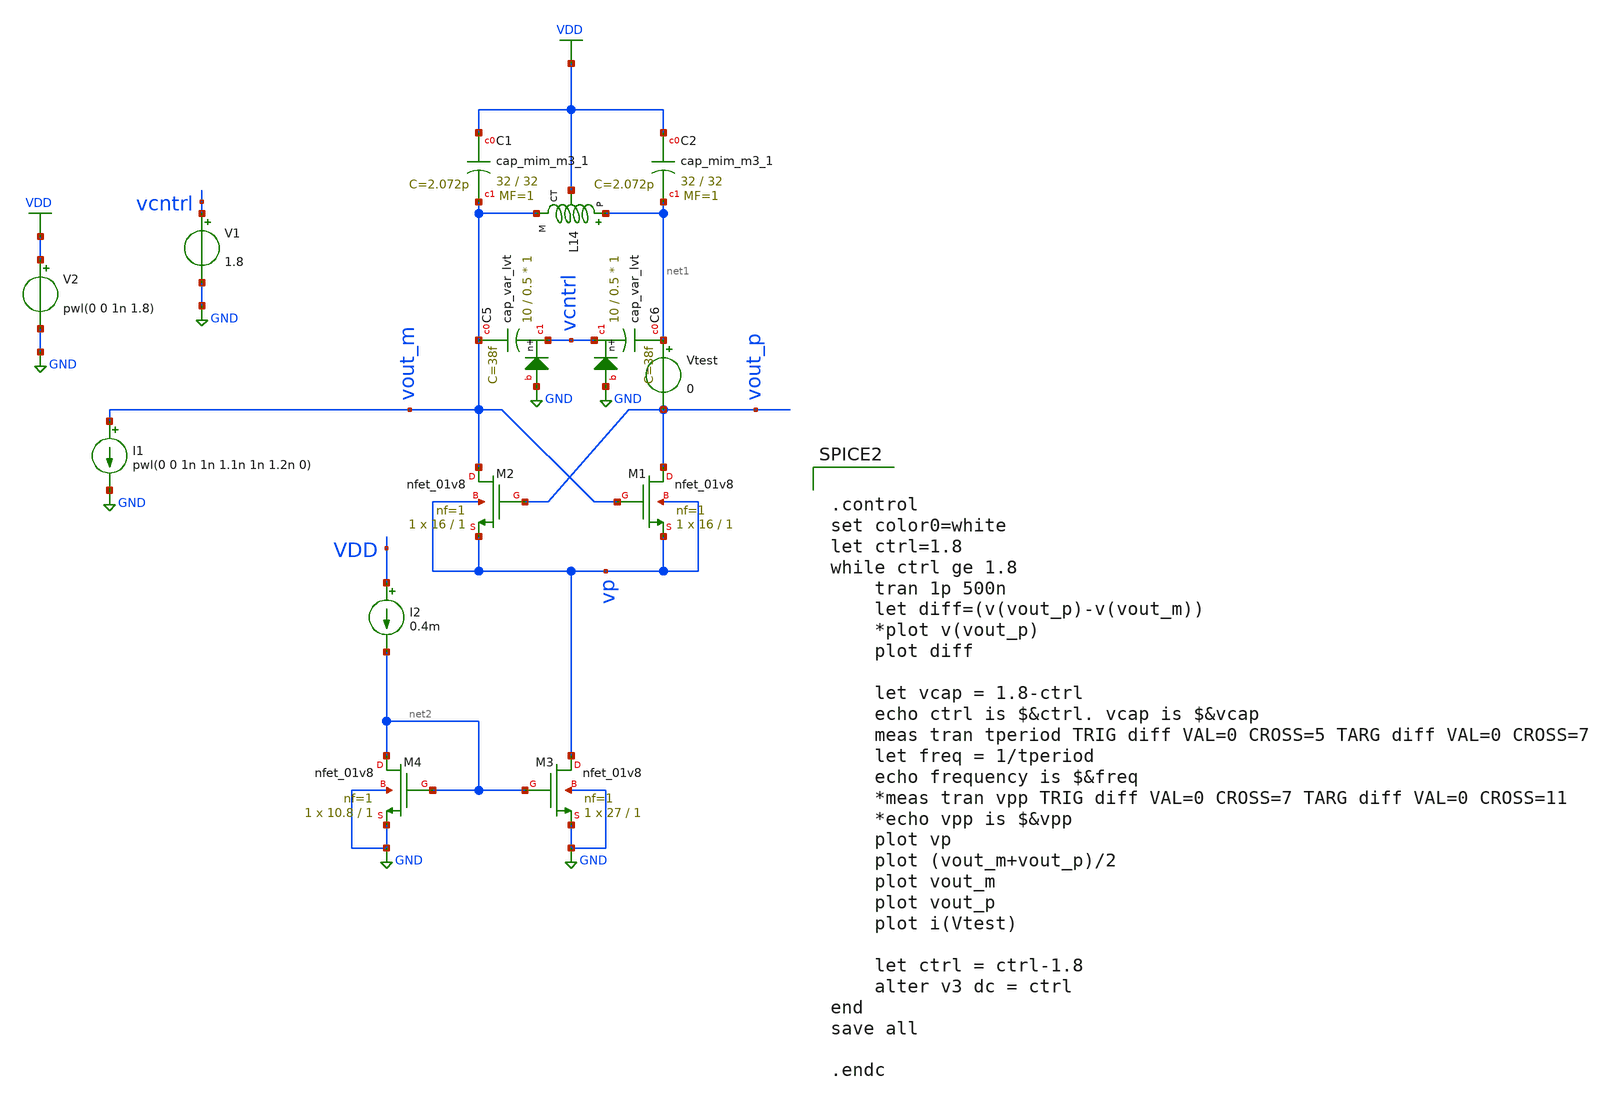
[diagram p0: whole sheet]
** sch_path: vco_cs.sch
**.subckt vco_cs
V2 VDD GND pwl(0 0 1n 1.8)
XC5 vout_m vcntrl GND sky130_fd_pr__cap_var_lvt W=10 L=0.5 VM=1 m=1
XC6 net1 vcntrl GND sky130_fd_pr__cap_var_lvt W=10 L=0.5 VM=1 m=1
I1 vout_m GND pwl(0 0 1n 1n 1.1n 1n 1.2n 0)
XM1 vout_p vout_m vp vp sky130_fd_pr__nfet_01v8 L=1 W=16 nf=1 ad='int((nf+1)/2) * W/nf * 0.29' as='int((nf+2)/2) * W/nf * 0.29'
+ pd='2*int((nf+1)/2) * (W/nf + 0.29)' ps='2*int((nf+2)/2) * (W/nf + 0.29)' nrd='0.29 / W' nrs='0.29 / W'
+ sa=0 sb=0 sd=0 mult=1 m=1
XM2 vout_m vout_p vp vp sky130_fd_pr__nfet_01v8 L=1 W=16 nf=1 ad='int((nf+1)/2) * W/nf * 0.29' as='int((nf+2)/2) * W/nf * 0.29'
+ pd='2*int((nf+1)/2) * (W/nf + 0.29)' ps='2*int((nf+2)/2) * (W/nf + 0.29)' nrd='0.29 / W' nrs='0.29 / W'
+ sa=0 sb=0 sd=0 mult=1 m=1
XC1 VDD vout_m sky130_fd_pr__cap_mim_m3_1 W=32 L=32 MF=1 m=1
XC2 VDD net1 sky130_fd_pr__cap_mim_m3_1 W=32 L=32 MF=1 m=1
XL14 net1 vout_m VDD GND sky130_fd_pr__ind_05_220
Vtest net1 vout_p 0
XM3 vp net2 GND GND sky130_fd_pr__nfet_01v8 L=1 W=27 nf=1 ad='int((nf+1)/2) * W/nf * 0.29' as='int((nf+2)/2) * W/nf * 0.29'
+ pd='2*int((nf+1)/2) * (W/nf + 0.29)' ps='2*int((nf+2)/2) * (W/nf + 0.29)' nrd='0.29 / W' nrs='0.29 / W'
+ sa=0 sb=0 sd=0 mult=1 m=1
XM4 net2 net2 GND GND sky130_fd_pr__nfet_01v8 L=1 W=10.8 nf=1 ad='int((nf+1)/2) * W/nf * 0.29' as='int((nf+2)/2) * W/nf * 0.29'
+ pd='2*int((nf+1)/2) * (W/nf + 0.29)' ps='2*int((nf+2)/2) * (W/nf + 0.29)' nrd='0.29 / W' nrs='0.29 / W'
+ sa=0 sb=0 sd=0 mult=1 m=1
I2 VDD net2 0.4m
V1 vcntrl GND 1.8
**** begin user architecture code


.option wnflag = 1
.lib /usr/local/share/pdk/sky130A/libs.tech/ngspice/sky130.lib.spice tt
.include /usr/local/share/pdk/sky130A/libs.ref/sky130_fd_pr/spice/sky130_fd_pr__ind_05_220.model.spice
.param mc_mm_switch=0




.control
set color0=white
let ctrl=1.8
while ctrl ge 1.8
	tran 1p 500n
	let diff=(v(vout_p)-v(vout_m))
	*plot v(vout_p)
	plot diff

	let vcap = 1.8-ctrl
	echo ctrl is $&ctrl. vcap is $&vcap
	meas tran tperiod TRIG diff VAL=0 CROSS=5 TARG diff VAL=0 CROSS=7
	let freq = 1/tperiod
	echo frequency is $&freq
	*meas tran vpp TRIG diff VAL=0 CROSS=7 TARG diff VAL=0 CROSS=11
	*echo vpp is $&vpp
	plot vp
	plot (vout_m+vout_p)/2
	plot vout_m
	plot vout_p
	plot i(Vtest)

	let ctrl = ctrl-1.8
	alter v3 dc = ctrl
end
save all

.endc


**** end user architecture code
**.ends
.GLOBAL VDD
.GLOBAL GND
.end
